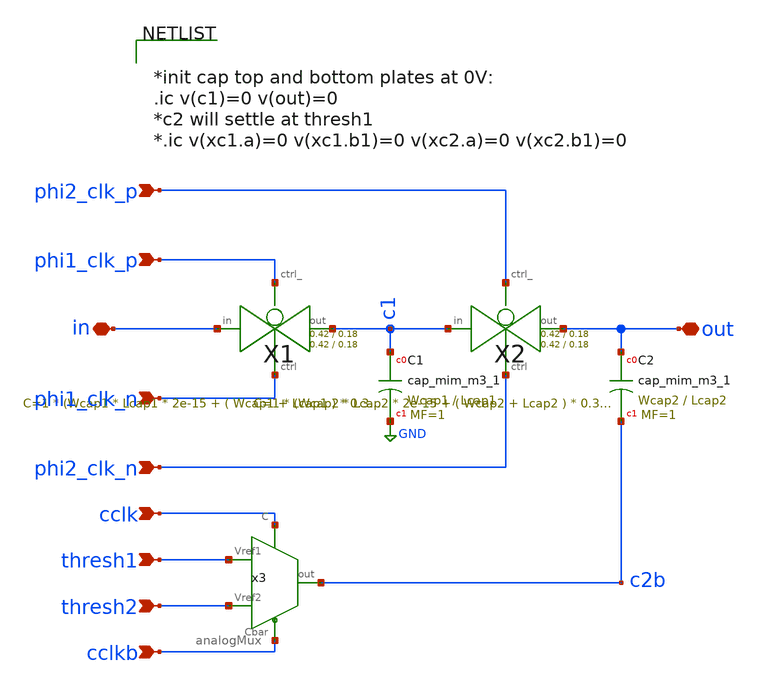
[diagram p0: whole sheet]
** sch_path: xschem/Switched_Caps/2switchcaps_thresh.sch
**.subckt 2switchcaps_thresh out in phi1_clk_n phi1_clk_p phi2_clk_p phi2_clk_n thresh1 cclk thresh2
*+ cclkb
*.iopin out
*.iopin in
*.ipin phi1_clk_n
*.ipin phi1_clk_p
*.ipin phi2_clk_p
*.ipin phi2_clk_n
*.ipin thresh1
*.ipin cclk
*.ipin thresh2
*.ipin cclkb
XC1 c1 GND sky130_fd_pr__cap_mim_m3_1 W=Wcap1 L=Lcap1 MF=1 m=1
XC2 out c2b sky130_fd_pr__cap_mim_m3_1 W=Wcap2 L=Lcap2 MF=1 m=1
X1 in c1 phi1_clk_p phi1_clk_n transmission_gate Wpmos=0.42 Lpmos=0.18 Wnmos=0.42 Lnmos=0.18
X2 c1 out phi2_clk_p phi2_clk_n transmission_gate Wpmos=0.42 Lpmos=0.18 Wnmos=0.42 Lnmos=0.18
x3 thresh2 thresh1 cclk cclkb c2b analogMux
**** begin user architecture code


*init cap top and bottom plates at 0V:
.ic v(c1)=0 v(out)=0
*c2 will settle at thresh1
*.ic v(xc1.a)=0 v(xc1.b1)=0 v(xc2.a)=0 v(xc2.b1)=0


**** end user architecture code
**.ends

* expanding   symbol:  transmission_gate/transmission_gate.sym # of pins=4
** sym_path: xschem/transmission_gate/transmission_gate.sym
** sch_path: xschem/transmission_gate/transmission_gate.sch
.subckt transmission_gate in out ctrl_ ctrl  Wpmos=0.42 Lpmos=0.18 Wnmos=0.42 Lnmos=0.18
*.iopin in
*.iopin out
*.ipin ctrl_
*.ipin ctrl
XM1 out ctrl in GND sky130_fd_pr__nfet_01v8 L=Lnmos W=Wnmos nf=1 ad='int((nf+1)/2) * W/nf * 0.29' as='int((nf+2)/2) * W/nf * 0.29'
+ pd='2*int((nf+1)/2) * (W/nf + 0.29)' ps='2*int((nf+2)/2) * (W/nf + 0.29)' nrd='0.29 / W' nrs='0.29 / W'
+ sa=0 sb=0 sd=0 mult=1 m=1
XM2 out ctrl_ in VDD sky130_fd_pr__pfet_01v8 L=Lpmos W=Wpmos nf=1 ad='int((nf+1)/2) * W/nf * 0.29' as='int((nf+2)/2) * W/nf * 0.29'
+ pd='2*int((nf+1)/2) * (W/nf + 0.29)' ps='2*int((nf+2)/2) * (W/nf + 0.29)' nrd='0.29 / W' nrs='0.29 / W'
+ sa=0 sb=0 sd=0 mult=1 m=1
.ends


* expanding   symbol:  comparator/analogMux.sym # of pins=5
** sym_path: xschem/comparator/analogMux.sym
** sch_path: xschem/comparator/analogMux.sch
.subckt analogMux Vref2 Vref1 C Cbar out
*.ipin Vref1
*.opin out
*.ipin Vref2
*.ipin C
*.ipin Cbar
XM1 Vref1 C out GND sky130_fd_pr__nfet_01v8 L=1 W=4 nf=1 ad='int((nf+1)/2) * W/nf * 0.29' as='int((nf+2)/2) * W/nf * 0.29'
+ pd='2*int((nf+1)/2) * (W/nf + 0.29)' ps='2*int((nf+2)/2) * (W/nf + 0.29)' nrd='0.29 / W' nrs='0.29 / W'
+ sa=0 sb=0 sd=0 mult=1 m=1
XM2 Vref1 Cbar out VDD sky130_fd_pr__pfet_01v8 L=1 W=8 nf=1 ad='int((nf+1)/2) * W/nf * 0.29' as='int((nf+2)/2) * W/nf * 0.29'
+ pd='2*int((nf+1)/2) * (W/nf + 0.29)' ps='2*int((nf+2)/2) * (W/nf + 0.29)' nrd='0.29 / W' nrs='0.29 / W'
+ sa=0 sb=0 sd=0 mult=1 m=1
XM3 out Cbar Vref2 GND sky130_fd_pr__nfet_01v8 L=1 W=4 nf=1 ad='int((nf+1)/2) * W/nf * 0.29' as='int((nf+2)/2) * W/nf * 0.29'
+ pd='2*int((nf+1)/2) * (W/nf + 0.29)' ps='2*int((nf+2)/2) * (W/nf + 0.29)' nrd='0.29 / W' nrs='0.29 / W'
+ sa=0 sb=0 sd=0 mult=1 m=1
XM4 out C Vref2 VDD sky130_fd_pr__pfet_01v8 L=1 W=8 nf=1 ad='int((nf+1)/2) * W/nf * 0.29' as='int((nf+2)/2) * W/nf * 0.29'
+ pd='2*int((nf+1)/2) * (W/nf + 0.29)' ps='2*int((nf+2)/2) * (W/nf + 0.29)' nrd='0.29 / W' nrs='0.29 / W'
+ sa=0 sb=0 sd=0 mult=1 m=1
.ends

.GLOBAL GND
.GLOBAL VDD
.end
